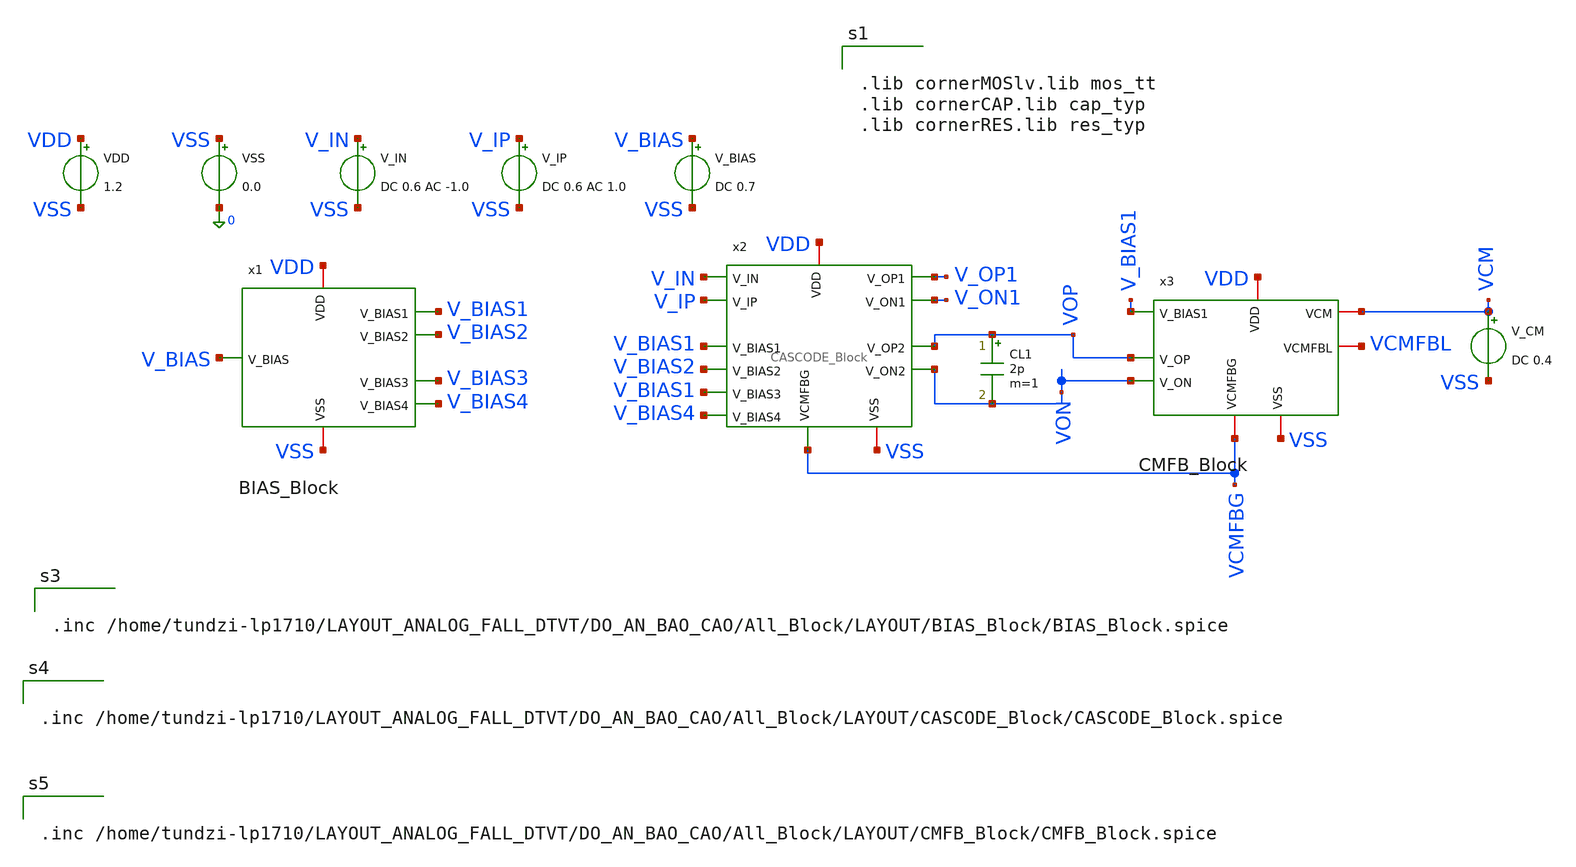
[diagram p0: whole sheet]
** sch_path: two-stage-ota-with-cmfb/Layout_PEX_PostSimulation/LAYOUT/SCHEMATIC_FOR_LAYOUT/AC_postSimulation.sch
**.subckt AC_postSimulation
VDD VDD VSS 1.2
VSS VSS 0 0.0
V_IN V_IN VSS DC 0.6 AC -1.0
V_IP V_IP VSS DC 0.6 AC 1.0
V_BIAS V_BIAS VSS DC 0.7
V_CM VCM VSS DC 0.4
CL1 VOP VON 2p m=1
x1 VDD VSS V_BIAS4 V_BIAS2 V_BIAS3 V_BIAS1 V_BIAS BIAS_Block
x2 VON VOP V_ON1 V_OP1 V_IN V_IP V_BIAS1 VSS V_BIAS4 V_BIAS1 VCMFBG VDD V_BIAS2 CASCODE_Block
x3 VDD V_BIAS1 VOP VON VCM VCMFBG VCMFBL VSS CMFB_Block
**** begin user architecture code


.lib cornerMOSlv.lib mos_tt
.lib cornerCAP.lib cap_typ
.lib cornerRES.lib res_typ




.inc /home/tundzi-lp1710/LAYOUT_ANALOG_FALL_DTVT/DO_AN_BAO_CAO/All_Block/LAYOUT/BIAS_Block/BIAS_Block.spice




.inc /home/tundzi-lp1710/LAYOUT_ANALOG_FALL_DTVT/DO_AN_BAO_CAO/All_Block/LAYOUT/CASCODE_Block/CASCODE_Block.spice




.inc /home/tundzi-lp1710/LAYOUT_ANALOG_FALL_DTVT/DO_AN_BAO_CAO/All_Block/LAYOUT/CMFB_Block/CMFB_Block.spice




* ==============================================================================
* TESTBENCH CHO MUC B: AC ANALYSIS (OPEN-LOOP, DIFFERENTIAL MODE)
* ==============================================================================

.control
set color0=white
set color1=black

echo '=========================================================================='
echo '  B1 & B2. DIFFERENTIAL OPEN-LOOP AC ANALYSIS (BODE, GAIN, GBW, PM, GM)  '
echo '=========================================================================='

* 1. Thiet lap nguon vi sai: vip = +0.5V, vin = -0.5V (Total AC input = 1V)
alter @v_ip[acmag] = 0.5
alter @v_in[acmag] = -0.5
alter @vdd[acmag]  = 0.0
alter @vss[acmag]  = 0.0

* Chay phan tich AC tu 1 Hz den 10 GHz (10 diem/decade)
ac dec 20 1 10G

* Tinh do loi vi sai (Magnitude va Phase)
let v_out_diff = v(vop) - v(von)
let gain_db = db(v_out_diff)
let phase_deg = (180 / pi) * unwrap(ph(v_out_diff))

setplot ac1
let avd_db = gain_db
let f_axis = frequency

* --- Tu dong trich xuat cac thong so dac trung ---
* 1. DC Gain (Av0 o tan so thap nhat f = 1Hz)
let av0 = gain_db[0]

* 2. Tim UGF / GBW (Tan so ma Gain = 0 dB)
meas ac gbw when gain_db=0

* 3. Tim Phase Margin (PM = Phase tai tan so UGF - (-180))
* Luu y: Voi OTA dao pha 180 do o tan so thap, PM thuong tinh bang: 180 + phase
meas ac phase_at_ugf find phase_deg when gain_db=0
let pm = 180 + phase_at_ugf

* 4. Tim Gain Margin (GM: Do sut giam Gain khi Pha cham -180 do)
meas ac f_180 when phase_deg=-180
meas ac gain_at_180 find gain_db when phase_deg=-180
let gm = -gain_at_180

echo '--------------------------------------------------------------------------'
echo '                    KET QUA TRICH XUAT OPEN-LOOP AC                       '
echo '--------------------------------------------------------------------------'
print av0
print gbw
print pm
print gm
echo '--------------------------------------------------------------------------'

* Ve do thi Bode Plot (Magnitude & Phase)
plot gain_db ylabel 'Magnitude (dB)' title 'Bode Plot: Differential Gain'
plot phase_deg ylabel 'Phase (Degrees)' title 'Bode Plot: Differential Phase'


echo '=========================================================================='
echo '  B3. COMMON-MODE REJECTION RATIO (CMRR vs. FREQUENCY)                   '
echo '=========================================================================='

* 2. Thiet lap nguon che do chung: vip = 1V, vin = 1V
alter @v_ip[acmag] = 1.0
alter @v_in[acmag] = 1.0
alter @vdd[acmag]  = 0.0
alter @vss[acmag]  = 0.0

ac dec 20 1 10G

* Do loi che do chung (Common-Mode Gain)
let v_out_cm = v(vop) - v(von)
let avc_db = db(v_out_cm)

* Tinh CMRR (dB) = Avd(dB) - Avc(dB)
let cmrr_db = ac1.avd_db - avc_db

meas ac cmrr_dc find cmrr_db at=1
meas ac cmrr_1mhz find cmrr_db at=1Meg

echo '--------------------------------------------------------------------------'
print cmrr_dc cmrr_1mhz
echo '--------------------------------------------------------------------------'

plot cmrr_db ylabel 'CMRR (dB)' title 'Common-Mode Rejection Ratio (CMRR) vs. Frequency'


echo '=========================================================================='
echo '  B3. POWER SUPPLY REJECTION RATIO (PSRR vs. FREQUENCY)                  '
echo '=========================================================================='

* --- a. PSRR cua nguon VDD ---
* Tat AC ngo vao, kich thich nguon VDD
alter @v_ip[acmag] = 0.0
alter @v_in[acmag] = 0.0
alter @vdd[acmag]  = 1.0
alter @vss[acmag]  = 0.0

ac dec 20 1 10G

let v_out_vdd = v(vop) - v(von)
let a_vdd_db = db(v_out_vdd)
let psrr_vdd_db = ac1.avd_db - a_vdd_db

meas ac psrr_vdd_dc find psrr_vdd_db at=1
meas ac psrr_vdd_1mhz find psrr_vdd_db at=1Meg

echo '--------------------------------------------------------------------------'
echo 'PSRR+ (VDD):'
print psrr_vdd_dc psrr_vdd_1mhz
echo '--------------------------------------------------------------------------'

plot psrr_vdd_db ylabel 'PSRR VDD (dB)' title 'PSRR+ (VDD) vs. Frequency'


* --- b. PSRR cua nguon VSS ---
* Tat AC VDD, kich thich nguon VSS
alter @vdd[acmag]  = 0.0
alter @vss[acmag]  = 1.0

ac dec 20 1 10G

let v_out_vss = v(vop) - v(von)
let a_vss_db = db(v_out_vss)
let psrr_vss_db = ac1.avd_db - a_vss_db

meas ac psrr_vss_dc find psrr_vss_db at=1
meas ac psrr_vss_1mhz find psrr_vss_db at=1Meg

echo '--------------------------------------------------------------------------'
echo 'PSRR- (VSS):'
print psrr_vss_dc psrr_vss_1mhz
echo '--------------------------------------------------------------------------'

plot psrr_vss_db ylabel 'PSRR VSS (dB)' title 'PSRR- (VSS) vs. Frequency'

.endc


**** end user architecture code
**.ends
.end
